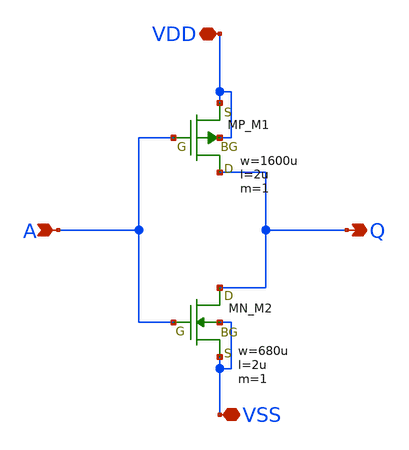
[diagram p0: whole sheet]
** sch_path: inverter/big/inverter_big.sch
**.subckt inverter_big A Q VDD VSS
*.ipin A
*.opin Q
*.iopin VDD
*.iopin VSS
XM1 Q A VDD VDD PMOS w=1600u l=2u as=0 ad=0 ps=0 pd=0 nrd=0 nrs=0 m=1
XM2 Q A VSS VSS NMOS w=680u l=2u as=0 ad=0 ps=0 pd=0 nrd=0 nrs=0 m=1
**.ends
.end
